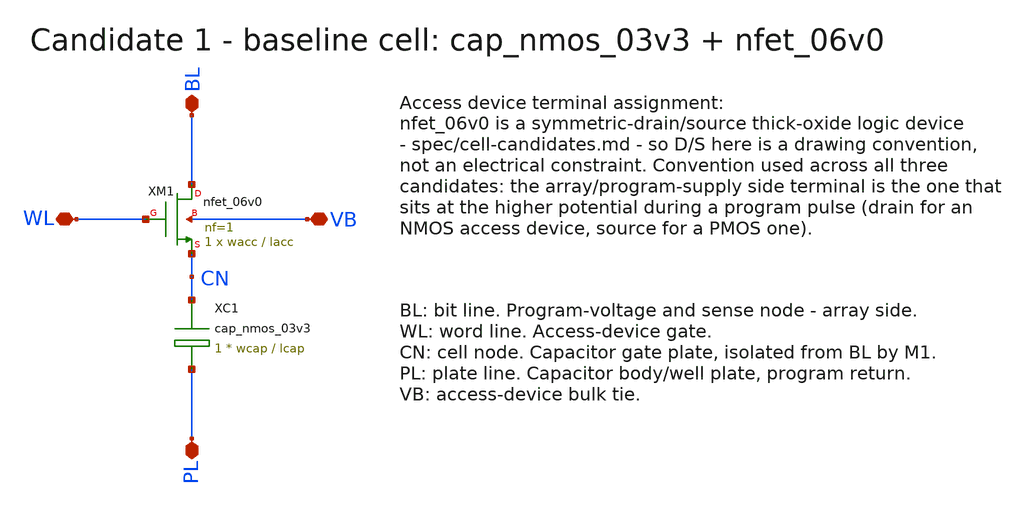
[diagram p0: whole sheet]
** sch_path: design/cells/cell_candidate1.sch
**.subckt cell_candidate1 BL WL PL VB
*.iopin BL
*.iopin WL
*.iopin PL
*.iopin VB
XM1 BL WL CN VB nfet_06v0 L=lacc W=wacc nf=1 ad='int((nf+1)/2) * wacc/nf * 0.18u' as='int((nf+2)/2) * wacc/nf * 0.18u'
+ pd='2*int((nf+1)/2) * (wacc/nf + 0.18u)' ps='2*int((nf+2)/2) * (wacc/nf + 0.18u)' nrd='0.18u / wacc'
+ nrs='0.18u / wacc' sa=0 sb=0 sd=0 m=1
XC1 CN PL cap_nmos_03v3 c_width=wcap c_length=lcap m=1
**.ends
.end
